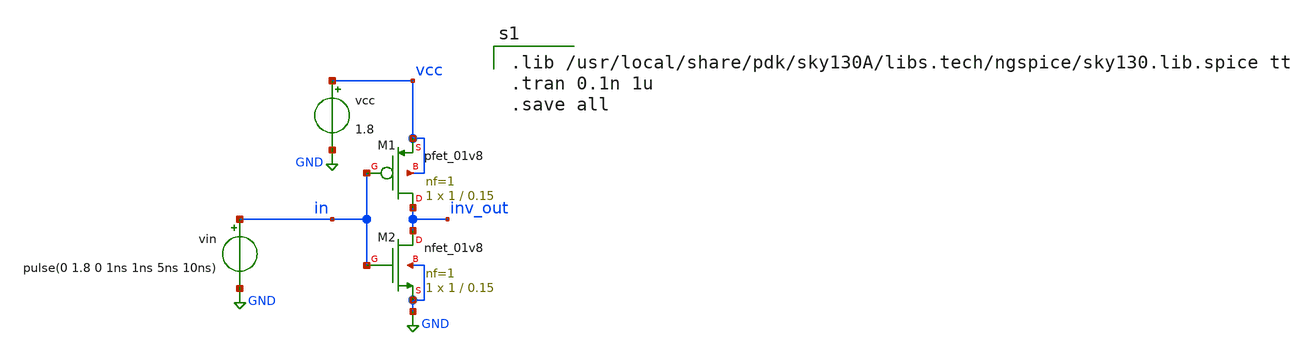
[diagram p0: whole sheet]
** sch_path: xschem_sky130/inverter.sch
**.subckt inverter
vcc vcc GND 1.8
XM1 inv_out in vcc vcc sky130_fd_pr__pfet_01v8 L=0.15 W=1 nf=1 ad='int((1 + 1)/2) * 1 / 1 * 0.29' as='int((1 + 2)/2) * 1 / 1 * 0.29'
+ pd='2*int((1 + 1)/2) * (1 / 1 + 0.29)' ps='2*int((1 + 2)/2) * (1 / 1 + 0.29)' nrd='0.29 / 1 ' nrs='0.29 / 1 '
+ sa=0 sb=0 sd=0 mult=1 m=1
XM2 inv_out in GND GND sky130_fd_pr__nfet_01v8 L=0.15 W=1 nf=1 ad='int((1 + 1)/2) * 1 / 1 * 0.29' as='int((1 + 2)/2) * 1 / 1 * 0.29'
+ pd='2*int((1 + 1)/2) * (1 / 1 + 0.29)' ps='2*int((1 + 2)/2) * (1 / 1 + 0.29)' nrd='0.29 / 1 ' nrs='0.29 / 1 '
+ sa=0 sb=0 sd=0 mult=1 m=1
vin in GND pulse(0 1.8 0 1ns 1ns 5ns 10ns)
**** begin user architecture code

.lib /usr/local/share/pdk/sky130A/libs.tech/ngspice/sky130.lib.spice tt
.tran 0.1n 1u
.save all

**** end user architecture code
**.ends
.GLOBAL GND
.end
